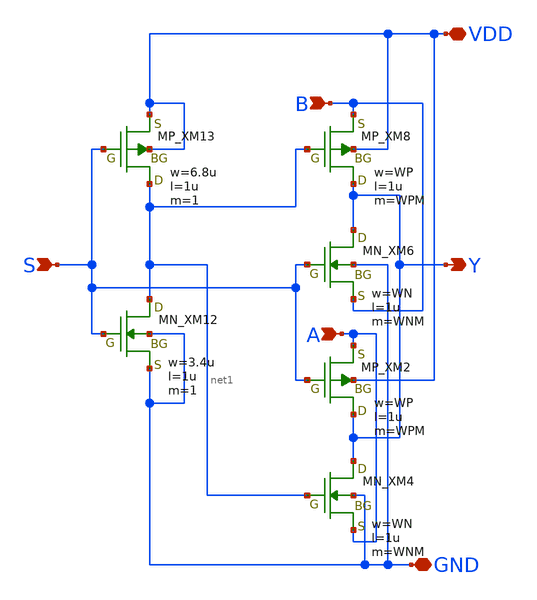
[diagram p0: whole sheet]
** sch_path: IO_202604/09/xschem/AMUX2_old.sch
**.subckt AMUX2_old B S Y VDD GND A
*.ipin B
*.ipin S
*.opin Y
*.iopin VDD
*.iopin GND
*.ipin A
XM13 net1 S VDD VDD PMOS w=6.8u l=1u as=0 ad=0 ps=0 pd=0 nrd=0 nrs=0 m=1
XM8 Y net1 B VDD PMOS w=WP l=1u as=0 ad=0 ps=0 pd=0 nrd=0 nrs=0 m=WPM
XM2 Y S A VDD PMOS w=WP l=1u as=0 ad=0 ps=0 pd=0 nrd=0 nrs=0 m=WPM
XM12 net1 S GND GND NMOS w=3.4u l=1u as=0 ad=0 ps=0 pd=0 nrd=0 nrs=0 m=1
XM6 Y S B GND NMOS w=WN l=1u as=0 ad=0 ps=0 pd=0 nrd=0 nrs=0 m=WNM
XM4 Y net1 A GND NMOS w=WN l=1u as=0 ad=0 ps=0 pd=0 nrd=0 nrs=0 m=WNM
**.ends
.end
